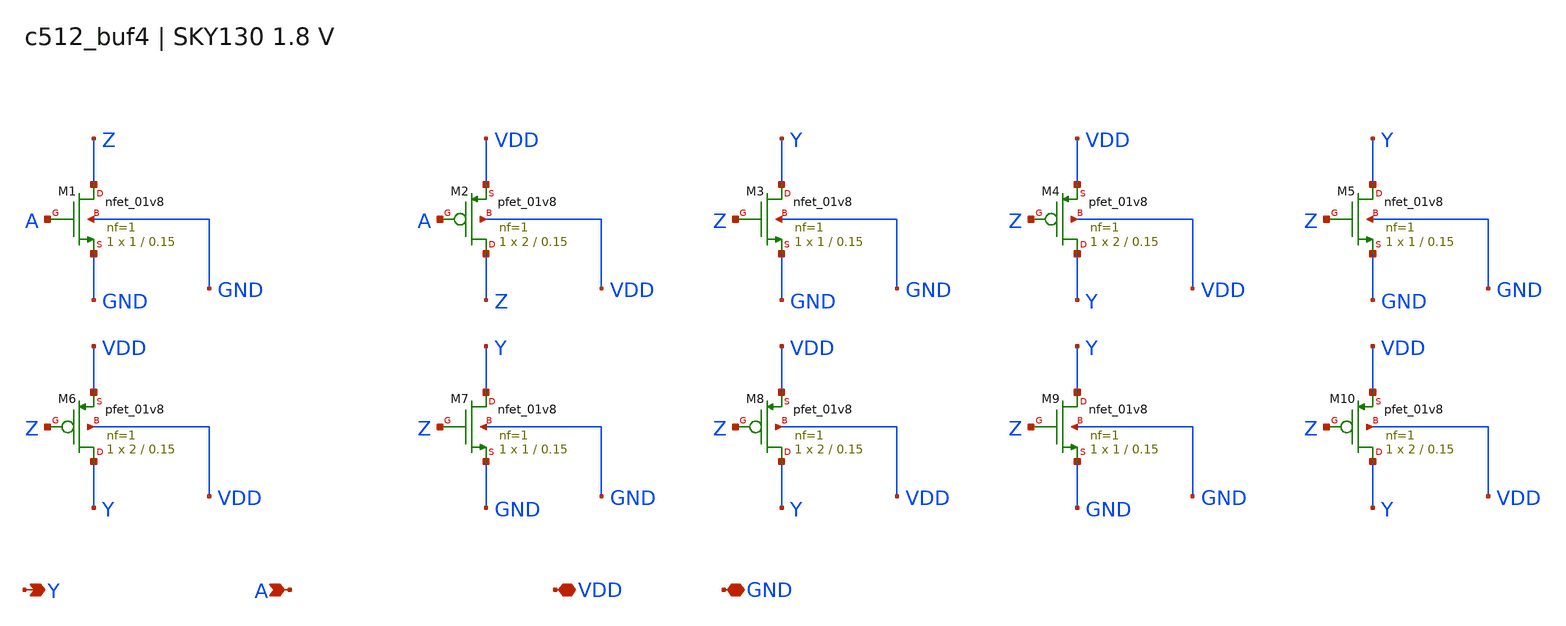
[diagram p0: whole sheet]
** sch_path: c512_buf4.sch
**.subckt c512_buf4 Y A VDD GND
*.opin Y
*.ipin A
*.iopin VDD
*.iopin GND
XM1 Z A GND GND sky130_fd_pr__nfet_01v8 L=0.15 W=1 nf=1 ad=0.29 as=0.29 pd=2.58 ps=2.58 nrd=0.29
+ nrs=0.29 sa=0 sb=0 sd=0 mult=1 m=1
XM2 Z A VDD VDD sky130_fd_pr__pfet_01v8 L=0.15 W=2 nf=1 ad=0.58 as=0.58 pd=4.58 ps=4.58 nrd=0.145
+ nrs=0.145 sa=0 sb=0 sd=0 mult=1 m=1
XM3 Y Z GND GND sky130_fd_pr__nfet_01v8 L=0.15 W=1 nf=1 ad=0.29 as=0.29 pd=2.58 ps=2.58 nrd=0.29
+ nrs=0.29 sa=0 sb=0 sd=0 mult=1 m=1
XM4 Y Z VDD VDD sky130_fd_pr__pfet_01v8 L=0.15 W=2 nf=1 ad=0.58 as=0.58 pd=4.58 ps=4.58 nrd=0.145
+ nrs=0.145 sa=0 sb=0 sd=0 mult=1 m=1
XM5 Y Z GND GND sky130_fd_pr__nfet_01v8 L=0.15 W=1 nf=1 ad=0.29 as=0.29 pd=2.58 ps=2.58 nrd=0.29
+ nrs=0.29 sa=0 sb=0 sd=0 mult=1 m=1
XM6 Y Z VDD VDD sky130_fd_pr__pfet_01v8 L=0.15 W=2 nf=1 ad=0.58 as=0.58 pd=4.58 ps=4.58 nrd=0.145
+ nrs=0.145 sa=0 sb=0 sd=0 mult=1 m=1
XM7 Y Z GND GND sky130_fd_pr__nfet_01v8 L=0.15 W=1 nf=1 ad=0.29 as=0.29 pd=2.58 ps=2.58 nrd=0.29
+ nrs=0.29 sa=0 sb=0 sd=0 mult=1 m=1
XM8 Y Z VDD VDD sky130_fd_pr__pfet_01v8 L=0.15 W=2 nf=1 ad=0.58 as=0.58 pd=4.58 ps=4.58 nrd=0.145
+ nrs=0.145 sa=0 sb=0 sd=0 mult=1 m=1
XM9 Y Z GND GND sky130_fd_pr__nfet_01v8 L=0.15 W=1 nf=1 ad=0.29 as=0.29 pd=2.58 ps=2.58 nrd=0.29
+ nrs=0.29 sa=0 sb=0 sd=0 mult=1 m=1
XM10 Y Z VDD VDD sky130_fd_pr__pfet_01v8 L=0.15 W=2 nf=1 ad=0.58 as=0.58 pd=4.58 ps=4.58 nrd=0.145
+ nrs=0.145 sa=0 sb=0 sd=0 mult=1 m=1
**.ends
.end
